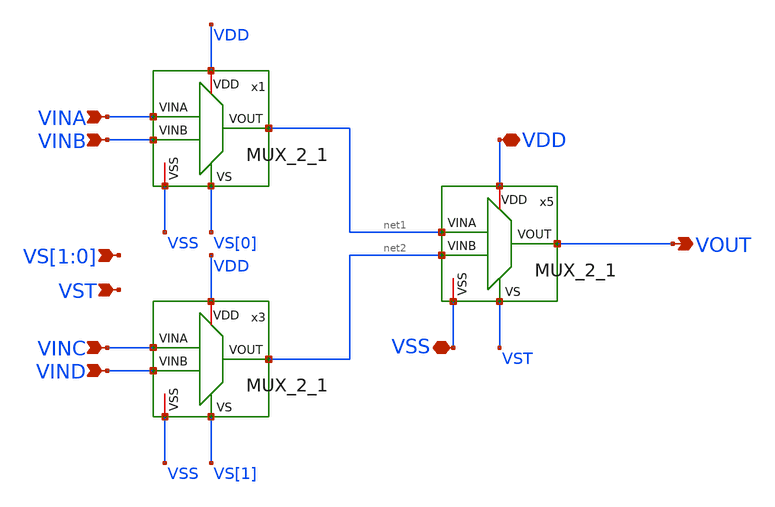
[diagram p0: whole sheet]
** sch_path: design/blocks-std-custom/MUX_4_1/schematic/MUX_4_1.sch
**.subckt MUX_4_1 VOUT VDD VSS VINA VINB VINC VIND VS[1],VS[0] VST
*.opin VOUT
*.iopin VDD
*.iopin VSS
*.ipin VINA
*.ipin VINB
*.ipin VINC
*.ipin VIND
*.ipin VS[1],VS[0]
*.ipin VST
x3 VDD VINC net2 VS[1] VIND VSS MUX_2_1
x5 VDD net1 VOUT VST net2 VSS MUX_2_1
x1 VDD VINA net1 VS[0] VINB VSS MUX_2_1
**.ends
.end
